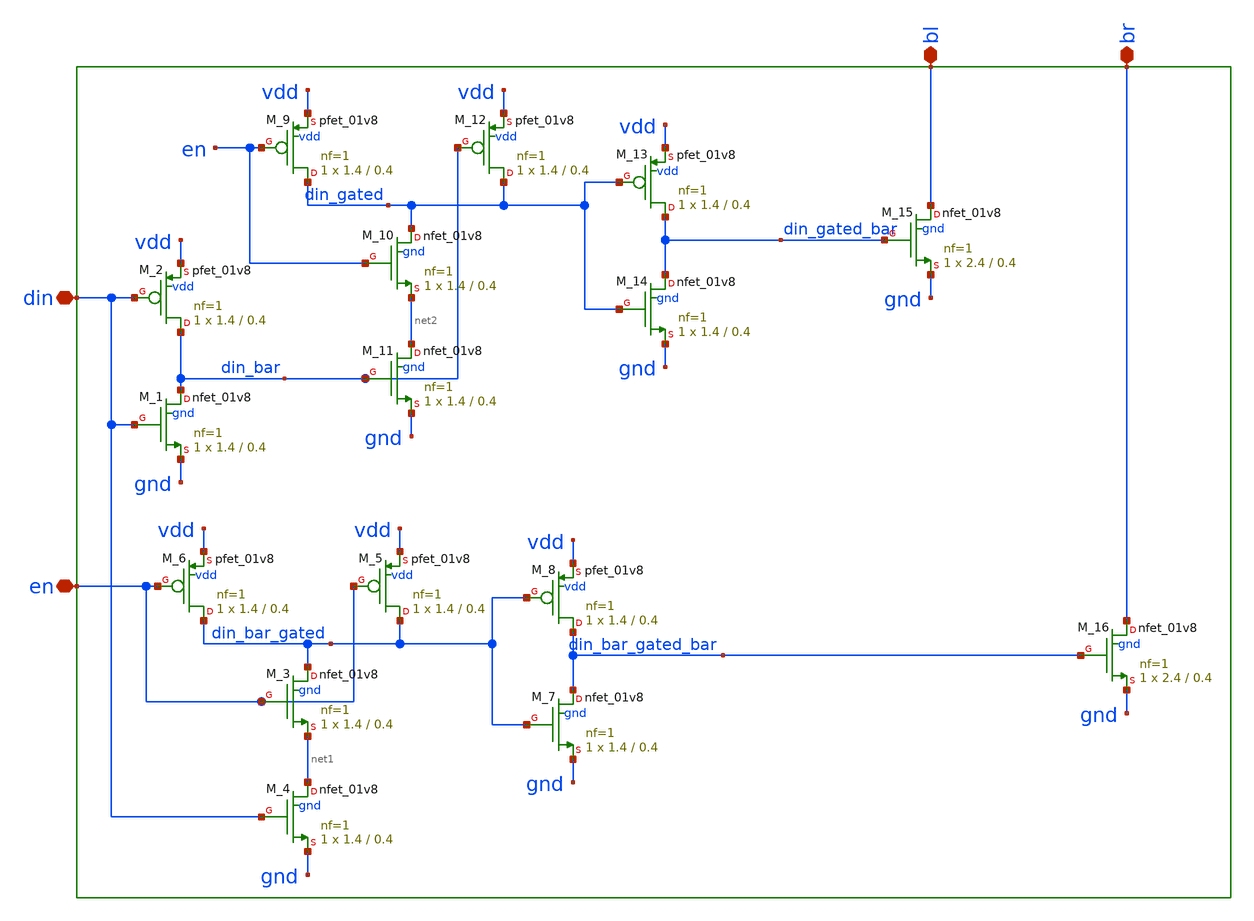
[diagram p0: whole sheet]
** sch_path: sram_2_64_scn4m_lcc/write_driver.sch
**.subckt write_driver din bl br en
*.iopin din
*.iopin bl
*.iopin br
*.iopin en
XM_1 din_bar din gnd gnd sky130_fd_pr__nfet_01v8 L=0.4 W=1.4 nf=1 ad='int((nf+1)/2) * W/nf * 0.29' as='int((nf+2)/2) * W/nf * 0.29'
+ pd='2*int((nf+1)/2) * (W/nf + 0.29)' ps='2*int((nf+2)/2) * (W/nf + 0.29)' nrd='0.29 / W' nrs='0.29 / W'
+ sa=0 sb=0 sd=0 mult=1 m=1
XM_2 din_bar din vdd vdd sky130_fd_pr__pfet_01v8 L=0.4 W=1.4 nf=1 ad='int((nf+1)/2) * W/nf * 0.29' as='int((nf+2)/2) * W/nf * 0.29'
+ pd='2*int((nf+1)/2) * (W/nf + 0.29)' ps='2*int((nf+2)/2) * (W/nf + 0.29)' nrd='0.29 / W' nrs='0.29 / W'
+ sa=0 sb=0 sd=0 mult=1 m=1
XM_6 din_bar_gated en vdd vdd sky130_fd_pr__pfet_01v8 L=0.4 W=1.4 nf=1 ad='int((nf+1)/2) * W/nf * 0.29'
+ as='int((nf+2)/2) * W/nf * 0.29' pd='2*int((nf+1)/2) * (W/nf + 0.29)' ps='2*int((nf+2)/2) * (W/nf + 0.29)'
+ nrd='0.29 / W' nrs='0.29 / W' sa=0 sb=0 sd=0 mult=1 m=1
XM_5 din_bar_gated en vdd vdd sky130_fd_pr__pfet_01v8 L=0.4 W=1.4 nf=1 ad='int((nf+1)/2) * W/nf * 0.29'
+ as='int((nf+2)/2) * W/nf * 0.29' pd='2*int((nf+1)/2) * (W/nf + 0.29)' ps='2*int((nf+2)/2) * (W/nf + 0.29)'
+ nrd='0.29 / W' nrs='0.29 / W' sa=0 sb=0 sd=0 mult=1 m=1
XM_3 din_bar_gated en net1 gnd sky130_fd_pr__nfet_01v8 L=0.4 W=1.4 nf=1 ad='int((nf+1)/2) * W/nf * 0.29'
+ as='int((nf+2)/2) * W/nf * 0.29' pd='2*int((nf+1)/2) * (W/nf + 0.29)' ps='2*int((nf+2)/2) * (W/nf + 0.29)'
+ nrd='0.29 / W' nrs='0.29 / W' sa=0 sb=0 sd=0 mult=1 m=1
XM_4 net1 din gnd gnd sky130_fd_pr__nfet_01v8 L=0.4 W=1.4 nf=1 ad='int((nf+1)/2) * W/nf * 0.29' as='int((nf+2)/2) * W/nf * 0.29'
+ pd='2*int((nf+1)/2) * (W/nf + 0.29)' ps='2*int((nf+2)/2) * (W/nf + 0.29)' nrd='0.29 / W' nrs='0.29 / W'
+ sa=0 sb=0 sd=0 mult=1 m=1
XM_7 din_bar_gated_bar din_bar_gated gnd gnd sky130_fd_pr__nfet_01v8 L=0.4 W=1.4 nf=1 ad='int((nf+1)/2) * W/nf * 0.29'
+ as='int((nf+2)/2) * W/nf * 0.29' pd='2*int((nf+1)/2) * (W/nf + 0.29)' ps='2*int((nf+2)/2) * (W/nf + 0.29)'
+ nrd='0.29 / W' nrs='0.29 / W' sa=0 sb=0 sd=0 mult=1 m=1
XM_8 din_bar_gated_bar din_bar_gated vdd vdd sky130_fd_pr__pfet_01v8 L=0.4 W=1.4 nf=1 ad='int((nf+1)/2) * W/nf * 0.29'
+ as='int((nf+2)/2) * W/nf * 0.29' pd='2*int((nf+1)/2) * (W/nf + 0.29)' ps='2*int((nf+2)/2) * (W/nf + 0.29)'
+ nrd='0.29 / W' nrs='0.29 / W' sa=0 sb=0 sd=0 mult=1 m=1
XM_9 din_gated en vdd vdd sky130_fd_pr__pfet_01v8 L=0.4 W=1.4 nf=1 ad='int((nf+1)/2) * W/nf * 0.29' as='int((nf+2)/2) * W/nf * 0.29'
+ pd='2*int((nf+1)/2) * (W/nf + 0.29)' ps='2*int((nf+2)/2) * (W/nf + 0.29)' nrd='0.29 / W' nrs='0.29 / W'
+ sa=0 sb=0 sd=0 mult=1 m=1
XM_12 din_gated din_bar vdd vdd sky130_fd_pr__pfet_01v8 L=0.4 W=1.4 nf=1 ad='int((nf+1)/2) * W/nf * 0.29'
+ as='int((nf+2)/2) * W/nf * 0.29' pd='2*int((nf+1)/2) * (W/nf + 0.29)' ps='2*int((nf+2)/2) * (W/nf + 0.29)'
+ nrd='0.29 / W' nrs='0.29 / W' sa=0 sb=0 sd=0 mult=1 m=1
XM_10 din_gated en net2 gnd sky130_fd_pr__nfet_01v8 L=0.4 W=1.4 nf=1 ad='int((nf+1)/2) * W/nf * 0.29'
+ as='int((nf+2)/2) * W/nf * 0.29' pd='2*int((nf+1)/2) * (W/nf + 0.29)' ps='2*int((nf+2)/2) * (W/nf + 0.29)'
+ nrd='0.29 / W' nrs='0.29 / W' sa=0 sb=0 sd=0 mult=1 m=1
XM_11 net2 din_bar gnd gnd sky130_fd_pr__nfet_01v8 L=0.4 W=1.4 nf=1 ad='int((nf+1)/2) * W/nf * 0.29'
+ as='int((nf+2)/2) * W/nf * 0.29' pd='2*int((nf+1)/2) * (W/nf + 0.29)' ps='2*int((nf+2)/2) * (W/nf + 0.29)'
+ nrd='0.29 / W' nrs='0.29 / W' sa=0 sb=0 sd=0 mult=1 m=1
XM_14 din_gated_bar din_gated gnd gnd sky130_fd_pr__nfet_01v8 L=0.4 W=1.4 nf=1 ad='int((nf+1)/2) * W/nf * 0.29'
+ as='int((nf+2)/2) * W/nf * 0.29' pd='2*int((nf+1)/2) * (W/nf + 0.29)' ps='2*int((nf+2)/2) * (W/nf + 0.29)'
+ nrd='0.29 / W' nrs='0.29 / W' sa=0 sb=0 sd=0 mult=1 m=1
XM_13 din_gated_bar din_gated vdd vdd sky130_fd_pr__pfet_01v8 L=0.4 W=1.4 nf=1 ad='int((nf+1)/2) * W/nf * 0.29'
+ as='int((nf+2)/2) * W/nf * 0.29' pd='2*int((nf+1)/2) * (W/nf + 0.29)' ps='2*int((nf+2)/2) * (W/nf + 0.29)'
+ nrd='0.29 / W' nrs='0.29 / W' sa=0 sb=0 sd=0 mult=1 m=1
XM_15 bl din_gated_bar gnd gnd sky130_fd_pr__nfet_01v8 L=0.4 W=2.4 nf=1 ad='int((nf+1)/2) * W/nf * 0.29'
+ as='int((nf+2)/2) * W/nf * 0.29' pd='2*int((nf+1)/2) * (W/nf + 0.29)' ps='2*int((nf+2)/2) * (W/nf + 0.29)'
+ nrd='0.29 / W' nrs='0.29 / W' sa=0 sb=0 sd=0 mult=1 m=1
XM_16 br din_bar_gated_bar gnd gnd sky130_fd_pr__nfet_01v8 L=0.4 W=2.4 nf=1 ad='int((nf+1)/2) * W/nf * 0.29'
+ as='int((nf+2)/2) * W/nf * 0.29' pd='2*int((nf+1)/2) * (W/nf + 0.29)' ps='2*int((nf+2)/2) * (W/nf + 0.29)'
+ nrd='0.29 / W' nrs='0.29 / W' sa=0 sb=0 sd=0 mult=1 m=1
**.ends
.end
